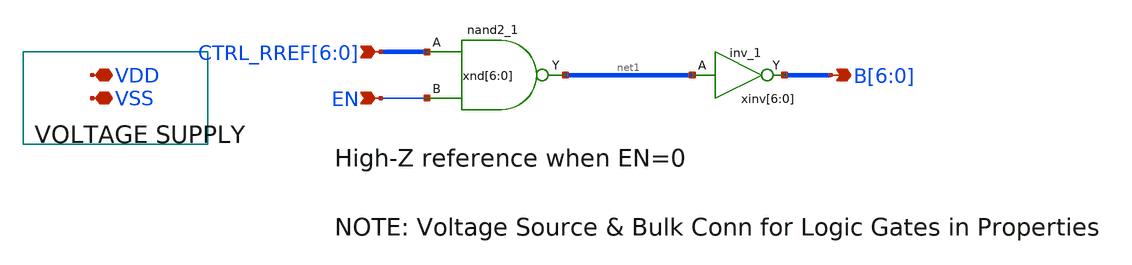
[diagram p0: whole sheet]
** sch_path: BL_Read_Interface/rram_read_csa_rref_digital.sch
**.subckt rram_read_csa_rref_digital VSS VDD
*+ CTRL_RREF[6],CTRL_RREF[5],CTRL_RREF[4],CTRL_RREF[3],CTRL_RREF[2],CTRL_RREF[1],CTRL_RREF[0] EN B[6],B[5],B[4],B[3],B[2],B[1],B[0]
*.iopin VSS
*.iopin VDD
*.ipin CTRL_RREF[6],CTRL_RREF[5],CTRL_RREF[4],CTRL_RREF[3],CTRL_RREF[2],CTRL_RREF[1],CTRL_RREF[0]
*.ipin EN
*.opin B[6],B[5],B[4],B[3],B[2],B[1],B[0]
xnd[6] CTRL_RREF[6] EN VSS VSS VDD VDD net1[6] sky130_fd_sc_hd__nand2_1
xnd[5] CTRL_RREF[5] EN VSS VSS VDD VDD net1[5] sky130_fd_sc_hd__nand2_1
xnd[4] CTRL_RREF[4] EN VSS VSS VDD VDD net1[4] sky130_fd_sc_hd__nand2_1
xnd[3] CTRL_RREF[3] EN VSS VSS VDD VDD net1[3] sky130_fd_sc_hd__nand2_1
xnd[2] CTRL_RREF[2] EN VSS VSS VDD VDD net1[2] sky130_fd_sc_hd__nand2_1
xnd[1] CTRL_RREF[1] EN VSS VSS VDD VDD net1[1] sky130_fd_sc_hd__nand2_1
xnd[0] CTRL_RREF[0] EN VSS VSS VDD VDD net1[0] sky130_fd_sc_hd__nand2_1
xinv[6] net1[6] VSS VSS VDD VDD B[6] sky130_fd_sc_hd__inv_1
xinv[5] net1[5] VSS VSS VDD VDD B[5] sky130_fd_sc_hd__inv_1
xinv[4] net1[4] VSS VSS VDD VDD B[4] sky130_fd_sc_hd__inv_1
xinv[3] net1[3] VSS VSS VDD VDD B[3] sky130_fd_sc_hd__inv_1
xinv[2] net1[2] VSS VSS VDD VDD B[2] sky130_fd_sc_hd__inv_1
xinv[1] net1[1] VSS VSS VDD VDD B[1] sky130_fd_sc_hd__inv_1
xinv[0] net1[0] VSS VSS VDD VDD B[0] sky130_fd_sc_hd__inv_1
**.ends
.end
